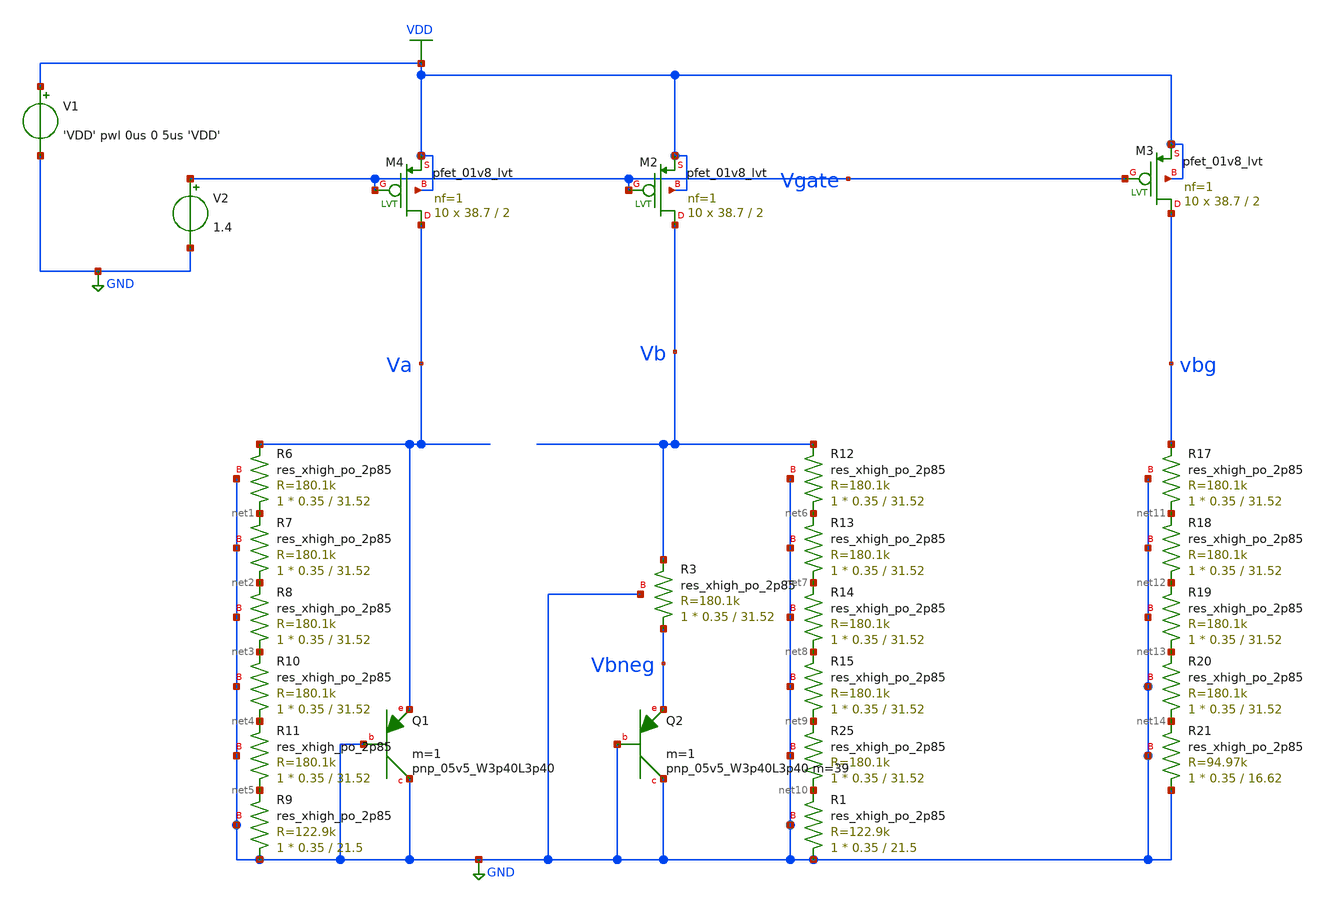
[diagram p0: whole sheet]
** sch_path: schematics/currentmirror_bandgapCore_test.sch
**.subckt currentmirror_bandgapCore_test
XR3 Vbneg Vb GND sky130_fd_pr__res_xhigh_po_2p85 L=31.52 mult=1 m=1
XR6 net1 Va GND sky130_fd_pr__res_xhigh_po_2p85 L=31.52 mult=1 m=1
XR7 net2 net1 GND sky130_fd_pr__res_xhigh_po_2p85 L=31.52 mult=1 m=1
XR8 net3 net2 GND sky130_fd_pr__res_xhigh_po_2p85 L=31.52 mult=1 m=1
XR10 net4 net3 GND sky130_fd_pr__res_xhigh_po_2p85 L=31.52 mult=1 m=1
XR11 net5 net4 GND sky130_fd_pr__res_xhigh_po_2p85 L=31.52 mult=1 m=1
XR9 GND net5 GND sky130_fd_pr__res_xhigh_po_2p85 L=21.5 mult=1 m=1
XR12 net6 Vb GND sky130_fd_pr__res_xhigh_po_2p85 L=31.52 mult=1 m=1
XR13 net7 net6 GND sky130_fd_pr__res_xhigh_po_2p85 L=31.52 mult=1 m=1
XR14 net8 net7 GND sky130_fd_pr__res_xhigh_po_2p85 L=31.52 mult=1 m=1
XR15 net9 net8 GND sky130_fd_pr__res_xhigh_po_2p85 L=31.52 mult=1 m=1
XR25 net10 net9 GND sky130_fd_pr__res_xhigh_po_2p85 L=31.52 mult=1 m=1
XR1 GND net10 GND sky130_fd_pr__res_xhigh_po_2p85 L=21.5 mult=1 m=1
XR17 net11 vbg GND sky130_fd_pr__res_xhigh_po_2p85 L=31.52 mult=1 m=1
XR18 net12 net11 GND sky130_fd_pr__res_xhigh_po_2p85 L=31.52 mult=1 m=1
XR19 net13 net12 GND sky130_fd_pr__res_xhigh_po_2p85 L=31.52 mult=1 m=1
XR20 net14 net13 GND sky130_fd_pr__res_xhigh_po_2p85 L=31.52 mult=1 m=1
XR21 GND net14 GND sky130_fd_pr__res_xhigh_po_2p85 L=16.62 mult=1 m=1
XQ1 GND GND Va sky130_fd_pr__pnp_05v5_W3p40L3p40 m=1
XQ2 GND GND Vbneg sky130_fd_pr__pnp_05v5_W3p40L3p40 m=39 m=1
XM2 Vb Vgate VDD VDD sky130_fd_pr__pfet_01v8_lvt L=2 W=38.7 nf=1 ad='int((nf+1)/2) * W/nf * 0.29' as='int((nf+2)/2) * W/nf * 0.29'
+ pd='2*int((nf+1)/2) * (W/nf + 0.29)' ps='2*int((nf+2)/2) * (W/nf + 0.29)' nrd='0.29 / W' nrs='0.29 / W'
+ sa=0 sb=0 sd=0 mult=10 m=10
XM3 vbg Vgate VDD VDD sky130_fd_pr__pfet_01v8_lvt L=2 W=38.7 nf=1 ad='int((nf+1)/2) * W/nf * 0.29' as='int((nf+2)/2) * W/nf * 0.29'
+ pd='2*int((nf+1)/2) * (W/nf + 0.29)' ps='2*int((nf+2)/2) * (W/nf + 0.29)' nrd='0.29 / W' nrs='0.29 / W'
+ sa=0 sb=0 sd=0 mult=10 m=10
XM4 Va Vgate VDD VDD sky130_fd_pr__pfet_01v8_lvt L=2 W=38.7 nf=1 ad='int((nf+1)/2) * W/nf * 0.29' as='int((nf+2)/2) * W/nf * 0.29'
+ pd='2*int((nf+1)/2) * (W/nf + 0.29)' ps='2*int((nf+2)/2) * (W/nf + 0.29)' nrd='0.29 / W' nrs='0.29 / W'
+ sa=0 sb=0 sd=0 mult=10 m=10
V1 VDD GND 'VDD' pwl 0us 0 5us 'VDD'
V2 Vgate GND 1.4
**** begin user architecture code

.include $::SKYWATER_MODELS/cells/nfet_01v8/sky130_fd_pr__nfet_01v8__tt.corner.spice
.include $::SKYWATER_MODELS/cells/nfet_01v8_lvt/sky130_fd_pr__nfet_01v8_lvt__tt.corner.spice
.include $::SKYWATER_MODELS/cells/pfet_01v8/sky130_fd_pr__pfet_01v8__tt.corner.spice
.include $::SKYWATER_MODELS/cells/nfet_03v3_nvt/sky130_fd_pr__nfet_03v3_nvt__tt.corner.spice
.include $::SKYWATER_MODELS/cells/nfet_05v0_nvt/sky130_fd_pr__nfet_05v0_nvt__tt.corner.spice
.include $::SKYWATER_MODELS/cells/esd_nfet_01v8/sky130_fd_pr__esd_nfet_01v8__tt.corner.spice
.include $::SKYWATER_MODELS/cells/pfet_01v8_lvt/sky130_fd_pr__pfet_01v8_lvt__tt.corner.spice
.include $::SKYWATER_MODELS/cells/pfet_01v8_hvt/sky130_fd_pr__pfet_01v8_hvt__tt.corner.spice
.include $::SKYWATER_MODELS/cells/esd_pfet_g5v0d10v5/sky130_fd_pr__esd_pfet_g5v0d10v5__tt.corner.spice
.include $::SKYWATER_MODELS/cells/pfet_g5v0d10v5/sky130_fd_pr__pfet_g5v0d10v5__tt.corner.spice
.include $::SKYWATER_MODELS/cells/pfet_g5v0d16v0/sky130_fd_pr__pfet_g5v0d16v0__tt.corner.spice
.include $::SKYWATER_MODELS/cells/nfet_g5v0d10v5/sky130_fd_pr__nfet_g5v0d10v5__tt.corner.spice
.include $::SKYWATER_MODELS/cells/nfet_g5v0d16v0/sky130_fd_pr__nfet_g5v0d16v0__tt_discrete.corner.spice
.include $::SKYWATER_MODELS/cells/esd_nfet_g5v0d10v5/sky130_fd_pr__esd_nfet_g5v0d10v5__tt.corner.spice
.include $::SKYWATER_MODELS/models/corners/tt/nonfet.spice
* Mismatch parameters
.include $::SKYWATER_MODELS/cells/nfet_01v8/sky130_fd_pr__nfet_01v8__mismatch.corner.spice
.include $::SKYWATER_MODELS/cells/pfet_01v8/sky130_fd_pr__pfet_01v8__mismatch.corner.spice
.include $::SKYWATER_MODELS/cells/nfet_01v8_lvt/sky130_fd_pr__nfet_01v8_lvt__mismatch.corner.spice
.include $::SKYWATER_MODELS/cells/pfet_01v8_lvt/sky130_fd_pr__pfet_01v8_lvt__mismatch.corner.spice
.include $::SKYWATER_MODELS/cells/pfet_01v8_hvt/sky130_fd_pr__pfet_01v8_hvt__mismatch.corner.spice
.include $::SKYWATER_MODELS/cells/nfet_g5v0d10v5/sky130_fd_pr__nfet_g5v0d10v5__mismatch.corner.spice
.include $::SKYWATER_MODELS/cells/pfet_g5v0d10v5/sky130_fd_pr__pfet_g5v0d10v5__mismatch.corner.spice
.include $::SKYWATER_MODELS/cells/nfet_05v0_nvt/sky130_fd_pr__nfet_05v0_nvt__mismatch.corner.spice
.include $::SKYWATER_MODELS/cells/nfet_03v3_nvt/sky130_fd_pr__nfet_03v3_nvt__mismatch.corner.spice
* Resistor$::SKYWATER_MODELS/Capacitor
.include $::SKYWATER_MODELS/models/r+c/res_typical__cap_typical.spice
.include $::SKYWATER_MODELS/models/r+c/res_typical__cap_typical__lin.spice
* Special cells
.include $::SKYWATER_MODELS/models/corners/tt/specialized_cells.spice
* All models
.include $::SKYWATER_MODELS/models/all.spice
*.include $::SKYWATER_MODELS/cells/pnp_05v5/sky130_fd_pr__pnp_05v5_W3p40L3p40.model.spice
.include /tmp/kustinj/ee272bclone/open_pdks/sky130A/libs.ref/sky130_fd_pr/spice/sky130_fd_pr__pnp_05v5_W3p40L3p40.model.spice
* Corner
.include $::SKYWATER_MODELS/models/corners/tt/rf.spice



.option savecurrents
.param mc_mm_switch=0
.param VDD=1.8

.control
save all  @m.xm1.msky130_fd_pr__pfet_01v8_lvt[gm]  @m.xm2.msky130_fd_pr__pfet_01v8_lvt[gm]
+  @m.xm3.msky130_fd_pr__pfet_01v8_lvt[gm]  @m.xm4.msky130_fd_pr__pfet_01v8_lvt[gm]  @m.xm5.msky130_fd_pr__nfet_01v8_lvt[gm]
+  @m.xm6.msky130_fd_pr__nfet_01v8_lvt[gm]  @m.xm7.msky130_fd_pr__nfet_01v8_lvt[gm]  @m.xm8.msky130_fd_pr__pfet_01v8_lvt[gm]
+  @m.xm9.msky130_fd_pr__nfet_01v8_lvt[gm]  @m.xm13.msky130_fd_pr__pfet_01v8_lvt[gm]

op
write currentmirror_bandgapCore_test.raw
let id8=@m.xm8.msky130_fd_pr__pfet_01v8_lvt[id]
let id1=@m.xm1.msky130_fd_pr__pfet_01v8_lvt[id]
let vth5=@m.xm5.msky130_fd_pr__nfet_01v8_lvt[vth]
let vth6=@m.xm6.msky130_fd_pr__nfet_01v8_lvt[vth]
let wm8=@m.xm8.msky130_fd_pr__pfet_01v8_lvt[w]
let mm8=@m.xm8.msky130_fd_pr__pfet_01v8_lvt[m]
let weff8=wm8*mm8
let jd8=id8/weff8
let wm1=@m.xm1.msky130_fd_pr__pfet_01v8_lvt[w]
let mm1=@m.xm1.msky130_fd_pr__pfet_01v8_lvt[m]
let weff1=wm1*mm1
let jd1=id1/weff1
let wm13=@m.xm13.msky130_fd_pr__pfet_01v8_lvt[w]
let mm13=@m.xm13.msky130_fd_pr__pfet_01v8_lvt[m]
let weff13=wm13*mm13
let id13=@m.xm13.msky130_fd_pr__pfet_01v8_lvt[id]
let jd13=id13/weff13
let gm13=@m.xm13.msky130_fd_pr__pfet_01v8_lvt[gm]
let gm3=@m.xm3.msky130_fd_pr__pfet_01v8_lvt[gm]
let gm4=@m.xm4.msky130_fd_pr__pfet_01v8_lvt[gm]
let gm5=@m.xm5.msky130_fd_pr__nfet_01v8_lvt[gm]
let gm6=@m.xm6.msky130_fd_pr__nfet_01v8_lvt[gm]
let gm7=@m.xm7.msky130_fd_pr__nfet_01v8_lvt[gm]
let gm8=@m.xm8.msky130_fd_pr__pfet_01v8_lvt[gm]
let gm9=@m.xm9.msky130_fd_pr__nfet_01v8_lvt[gm]
let gm1=@m.xm1.msky130_fd_pr__pfet_01v8_lvt[gm]
let gm2=@m.xm2.msky130_fd_pr__pfet_01v8_lvt[gm]
let vdsat1=2/(gm1/vm1#branch)
let vdsat2=2/(gm2/vm2#branch)
let vdsat3=2/(gm3/vm3#branch)
let vdsat4=2/(gm4/@m.xm4.msky130_fd_pr__pfet_01v8_lvt[id])
let vdsat5=2/(gm5/@m.xm5.msky130_fd_pr__nfet_01v8_lvt[id])
let vdsat6=2/(gm6/@m.xm6.msky130_fd_pr__nfet_01v8_lvt[id])
let vdsat7=2/(gm7/@m.xm7.msky130_fd_pr__nfet_01v8_lvt[id])
let vdsat8=2/(gm8/@m.xm8.msky130_fd_pr__pfet_01v8_lvt[id])
let vdsat9=2/(gm9/@m.xm9.msky130_fd_pr__nfet_01v8_lvt[id])
let vdsat13=2/(gm13/@m.xm13.msky130_fd_pr__pfet_01v8_lvt[id])


print vbg vgate vg va vb vx vq
print vdsat1 vdsat2 vdsat3 vdsat4   vdsat5 vdsat6 vdsat7 vdsat8 vdsat9 vdsat13
.endc


**** end user architecture code
**.ends
.GLOBAL GND
.GLOBAL VDD
.end
